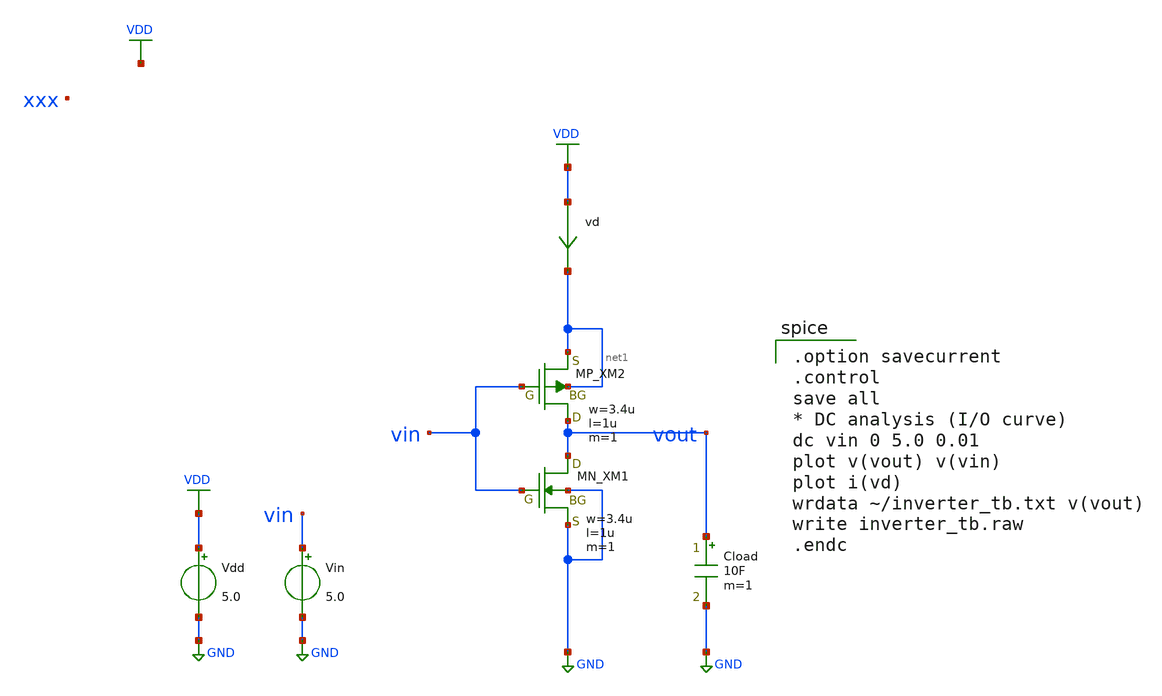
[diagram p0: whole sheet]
** sch_path: inverter/inverter_Shusuke_Isimaru_tb.sch
**.subckt inverter_Shusuke_Isimaru_tb
XXM1 vout vin GND GND NMOS w=3.4u l=1u nrd=0 nrs=0 m=1
XXM2 vout vin net1 net1 PMOS w=3.4u l=1u nrd=0 nrs=0 m=1
Vdd VDD GND 5.0
Vin vin GND 5.0
vd VDD net1 0
.save i(vd)
Cload vout GND 10F m=1
**** begin user architecture code
 .include $::LIB/ip62_models

.option savecurrent
.control
save all
* DC analysis (I/O curve)
dc vin 0 5.0 0.01
plot v(vout) v(vin)
plot i(vd)
wrdata ~/inverter_tb.txt v(vout)
write inverter_tb.raw
.endc

**** end user architecture code
**.ends
.GLOBAL GND
.GLOBAL VDD
.end
